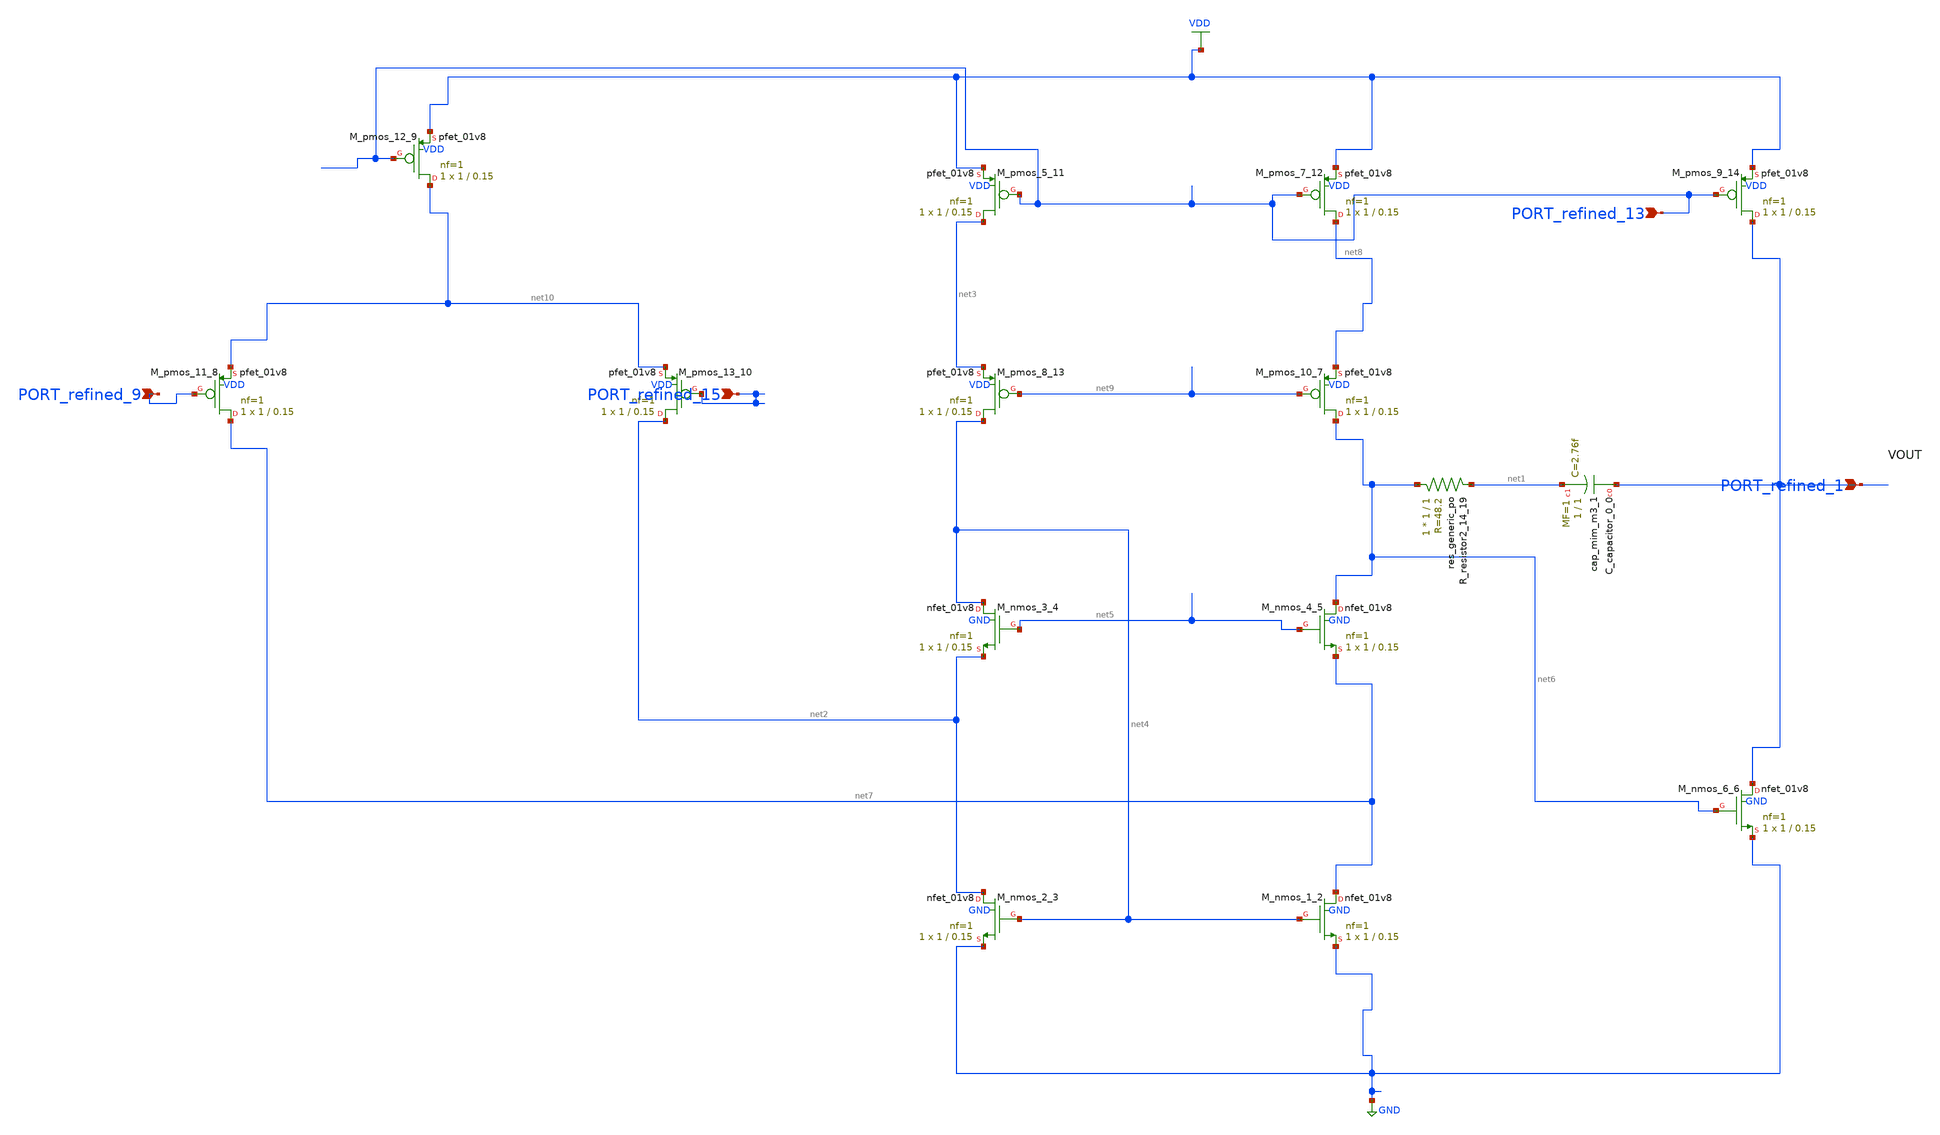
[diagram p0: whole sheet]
** sch_path: schematics/p09_folded_cascode_opamp.sch
**.subckt p09_folded_cascode_opamp PORT_refined_9 PORT_refined_13 PORT_refined_15 PORT_refined_1
*.ipin PORT_refined_9
*.ipin PORT_refined_13
*.ipin PORT_refined_15
*.ipin PORT_refined_1
XC_capacitor_0_0 PORT_refined_1 net1 sky130_fd_pr__cap_mim_m3_1 W=1 L=1 MF=1 m=1
XM_nmos_1_2 net7 net4 GND GND sky130_fd_pr__nfet_01v8 L=0.15 W=1 nf=1 ad='int((1 + 1)/2) * 1 / 1 * 0.29'
+ as='int((1 + 2)/2) * 1 / 1 * 0.29' pd='2*int((1 + 1)/2) * (1 / 1 + 0.29)' ps='2*int((1 + 2)/2) * (1 / 1 + 0.29)'
+ nrd='0.29 / 1 ' nrs='0.29 / 1 ' sa=0 sb=0 sd=0 mult=1 m=1
XM_nmos_2_3 net2 net4 GND GND sky130_fd_pr__nfet_01v8 L=0.15 W=1 nf=1 ad='int((1 + 1)/2) * 1 / 1 * 0.29'
+ as='int((1 + 2)/2) * 1 / 1 * 0.29' pd='2*int((1 + 1)/2) * (1 / 1 + 0.29)' ps='2*int((1 + 2)/2) * (1 / 1 + 0.29)'
+ nrd='0.29 / 1 ' nrs='0.29 / 1 ' sa=0 sb=0 sd=0 mult=1 m=1
XM_nmos_3_4 net4 net5 net2 GND sky130_fd_pr__nfet_01v8 L=0.15 W=1 nf=1 ad='int((1 + 1)/2) * 1 / 1 * 0.29'
+ as='int((1 + 2)/2) * 1 / 1 * 0.29' pd='2*int((1 + 1)/2) * (1 / 1 + 0.29)' ps='2*int((1 + 2)/2) * (1 / 1 + 0.29)'
+ nrd='0.29 / 1 ' nrs='0.29 / 1 ' sa=0 sb=0 sd=0 mult=1 m=1
XM_nmos_4_5 net6 net5 net7 GND sky130_fd_pr__nfet_01v8 L=0.15 W=1 nf=1 ad='int((1 + 1)/2) * 1 / 1 * 0.29'
+ as='int((1 + 2)/2) * 1 / 1 * 0.29' pd='2*int((1 + 1)/2) * (1 / 1 + 0.29)' ps='2*int((1 + 2)/2) * (1 / 1 + 0.29)'
+ nrd='0.29 / 1 ' nrs='0.29 / 1 ' sa=0 sb=0 sd=0 mult=1 m=1
XM_nmos_6_6 PORT_refined_1 net6 GND GND sky130_fd_pr__nfet_01v8 L=0.15 W=1 nf=1 ad='int((1 + 1)/2) * 1 / 1 * 0.29'
+ as='int((1 + 2)/2) * 1 / 1 * 0.29' pd='2*int((1 + 1)/2) * (1 / 1 + 0.29)' ps='2*int((1 + 2)/2) * (1 / 1 + 0.29)'
+ nrd='0.29 / 1 ' nrs='0.29 / 1 ' sa=0 sb=0 sd=0 mult=1 m=1
XM_pmos_10_7 net6 net9 net8 VDD sky130_fd_pr__pfet_01v8 L=0.15 W=1 nf=1 ad='int((1 + 1)/2) * 1 / 1 * 0.29'
+ as='int((1 + 2)/2) * 1 / 1 * 0.29' pd='2*int((1 + 1)/2) * (1 / 1 + 0.29)' ps='2*int((1 + 2)/2) * (1 / 1 + 0.29)'
+ nrd='0.29 / 1 ' nrs='0.29 / 1 ' sa=0 sb=0 sd=0 mult=1 m=1
XM_pmos_11_8 net7 PORT_refined_9 net10 VDD sky130_fd_pr__pfet_01v8 L=0.15 W=1 nf=1 ad='int((1 + 1)/2) * 1 / 1 * 0.29'
+ as='int((1 + 2)/2) * 1 / 1 * 0.29' pd='2*int((1 + 1)/2) * (1 / 1 + 0.29)' ps='2*int((1 + 2)/2) * (1 / 1 + 0.29)'
+ nrd='0.29 / 1 ' nrs='0.29 / 1 ' sa=0 sb=0 sd=0 mult=1 m=1
XM_pmos_12_9 net10 PORT_refined_13 VDD VDD sky130_fd_pr__pfet_01v8 L=0.15 W=1 nf=1 ad='int((1 + 1)/2) * 1 / 1 * 0.29'
+ as='int((1 + 2)/2) * 1 / 1 * 0.29' pd='2*int((1 + 1)/2) * (1 / 1 + 0.29)' ps='2*int((1 + 2)/2) * (1 / 1 + 0.29)'
+ nrd='0.29 / 1 ' nrs='0.29 / 1 ' sa=0 sb=0 sd=0 mult=1 m=1
XM_pmos_13_10 net2 PORT_refined_15 net10 VDD sky130_fd_pr__pfet_01v8 L=0.15 W=1 nf=1 ad='int((1 + 1)/2) * 1 / 1 * 0.29'
+ as='int((1 + 2)/2) * 1 / 1 * 0.29' pd='2*int((1 + 1)/2) * (1 / 1 + 0.29)' ps='2*int((1 + 2)/2) * (1 / 1 + 0.29)'
+ nrd='0.29 / 1 ' nrs='0.29 / 1 ' sa=0 sb=0 sd=0 mult=1 m=1
XM_pmos_5_11 net3 PORT_refined_13 VDD VDD sky130_fd_pr__pfet_01v8 L=0.15 W=1 nf=1 ad='int((1 + 1)/2) * 1 / 1 * 0.29'
+ as='int((1 + 2)/2) * 1 / 1 * 0.29' pd='2*int((1 + 1)/2) * (1 / 1 + 0.29)' ps='2*int((1 + 2)/2) * (1 / 1 + 0.29)'
+ nrd='0.29 / 1 ' nrs='0.29 / 1 ' sa=0 sb=0 sd=0 mult=1 m=1
XM_pmos_7_12 net8 PORT_refined_13 VDD VDD sky130_fd_pr__pfet_01v8 L=0.15 W=1 nf=1 ad='int((1 + 1)/2) * 1 / 1 * 0.29'
+ as='int((1 + 2)/2) * 1 / 1 * 0.29' pd='2*int((1 + 1)/2) * (1 / 1 + 0.29)' ps='2*int((1 + 2)/2) * (1 / 1 + 0.29)'
+ nrd='0.29 / 1 ' nrs='0.29 / 1 ' sa=0 sb=0 sd=0 mult=1 m=1
XM_pmos_8_13 net4 net9 net3 VDD sky130_fd_pr__pfet_01v8 L=0.15 W=1 nf=1 ad='int((1 + 1)/2) * 1 / 1 * 0.29'
+ as='int((1 + 2)/2) * 1 / 1 * 0.29' pd='2*int((1 + 1)/2) * (1 / 1 + 0.29)' ps='2*int((1 + 2)/2) * (1 / 1 + 0.29)'
+ nrd='0.29 / 1 ' nrs='0.29 / 1 ' sa=0 sb=0 sd=0 mult=1 m=1
XM_pmos_9_14 PORT_refined_1 PORT_refined_13 VDD VDD sky130_fd_pr__pfet_01v8 L=0.15 W=1 nf=1 ad='int((1 + 1)/2) * 1 / 1 * 0.29'
+ as='int((1 + 2)/2) * 1 / 1 * 0.29' pd='2*int((1 + 1)/2) * (1 / 1 + 0.29)' ps='2*int((1 + 2)/2) * (1 / 1 + 0.29)'
+ nrd='0.29 / 1 ' nrs='0.29 / 1 ' sa=0 sb=0 sd=0 mult=1 m=1
XR_resistor2_14_19 net6 net1 sky130_fd_pr__res_generic_po W=1 L=1 m=1
**.ends
.GLOBAL GND
.GLOBAL VDD
.end
